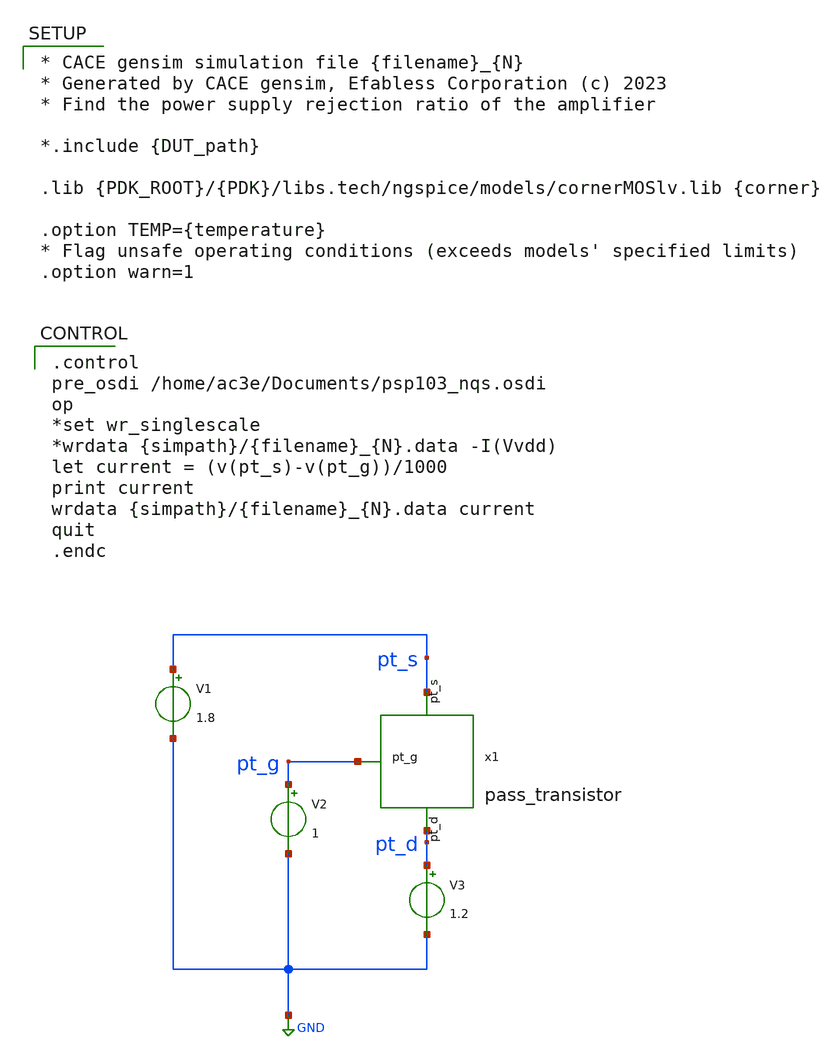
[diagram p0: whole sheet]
** sch_path: AC3E-IHP_ALDO/val/cace/pass_transistor_current.sch
**.subckt pass_transistor_current
x1 pt_g pt_s pt_d pass_transistor
V1 pt_s GND 1.8
V3 pt_d GND 1.2
V2 pt_g GND 1
**** begin user architecture code

* CACE gensim simulation file {filename}_{N}
* Generated by CACE gensim, Efabless Corporation (c) 2023
* Find the power supply rejection ratio of the amplifier

*.include {DUT_path}

.lib {PDK_ROOT}/{PDK}/libs.tech/ngspice/models/cornerMOSlv.lib {corner}

.option TEMP={temperature}
* Flag unsafe operating conditions (exceeds models' specified limits)
.option warn=1



.control
pre_osdi /home/ac3e/Documents/psp103_nqs.osdi
op
*set wr_singlescale
*wrdata {simpath}/{filename}_{N}.data -I(Vvdd)
let current = (v(pt_s)-v(pt_g))/1000
print current
wrdata {simpath}/{filename}_{N}.data current
quit
.endc


**** end user architecture code
**.ends
.GLOBAL GND
.end
